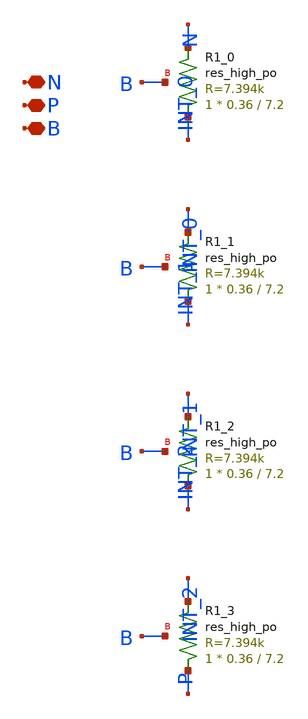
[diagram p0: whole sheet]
** sch_path: design/LELO_TEMP_SKY130A/REYATR_RES4.sch
**.subckt REYATR_RES4 N P B
*.iopin N
*.iopin P
*.iopin B
XR1_0 INT_0 N B sky130_fd_pr__res_high_po W=0.36 L=7.2 mult=1 m=1
XR1_1 INT_1 INT_0 B sky130_fd_pr__res_high_po W=0.36 L=7.2 mult=1 m=1
XR1_2 INT_2 INT_1 B sky130_fd_pr__res_high_po W=0.36 L=7.2 mult=1 m=1
XR1_3 P INT_2 B sky130_fd_pr__res_high_po W=0.36 L=7.2 mult=1 m=1
**.ends
.end
